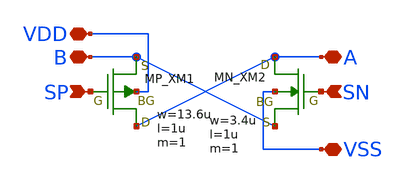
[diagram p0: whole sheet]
** sch_path: member_project/Charactorization/ShuntaroOHNO/cells/TG.sch
**.subckt TG A B VDD VSS SP SN
*.iopin A
*.iopin B
*.iopin VDD
*.iopin VSS
*.ipin SP
*.ipin SN
XXM1 A SP B VDD PMOS w=13.6u l=1u nrd=0 nrs=0 m=1
XXM2 A SN B VSS NMOS w=3.4u l=1u nrd=0 nrs=0 m=1
**.ends
.end
